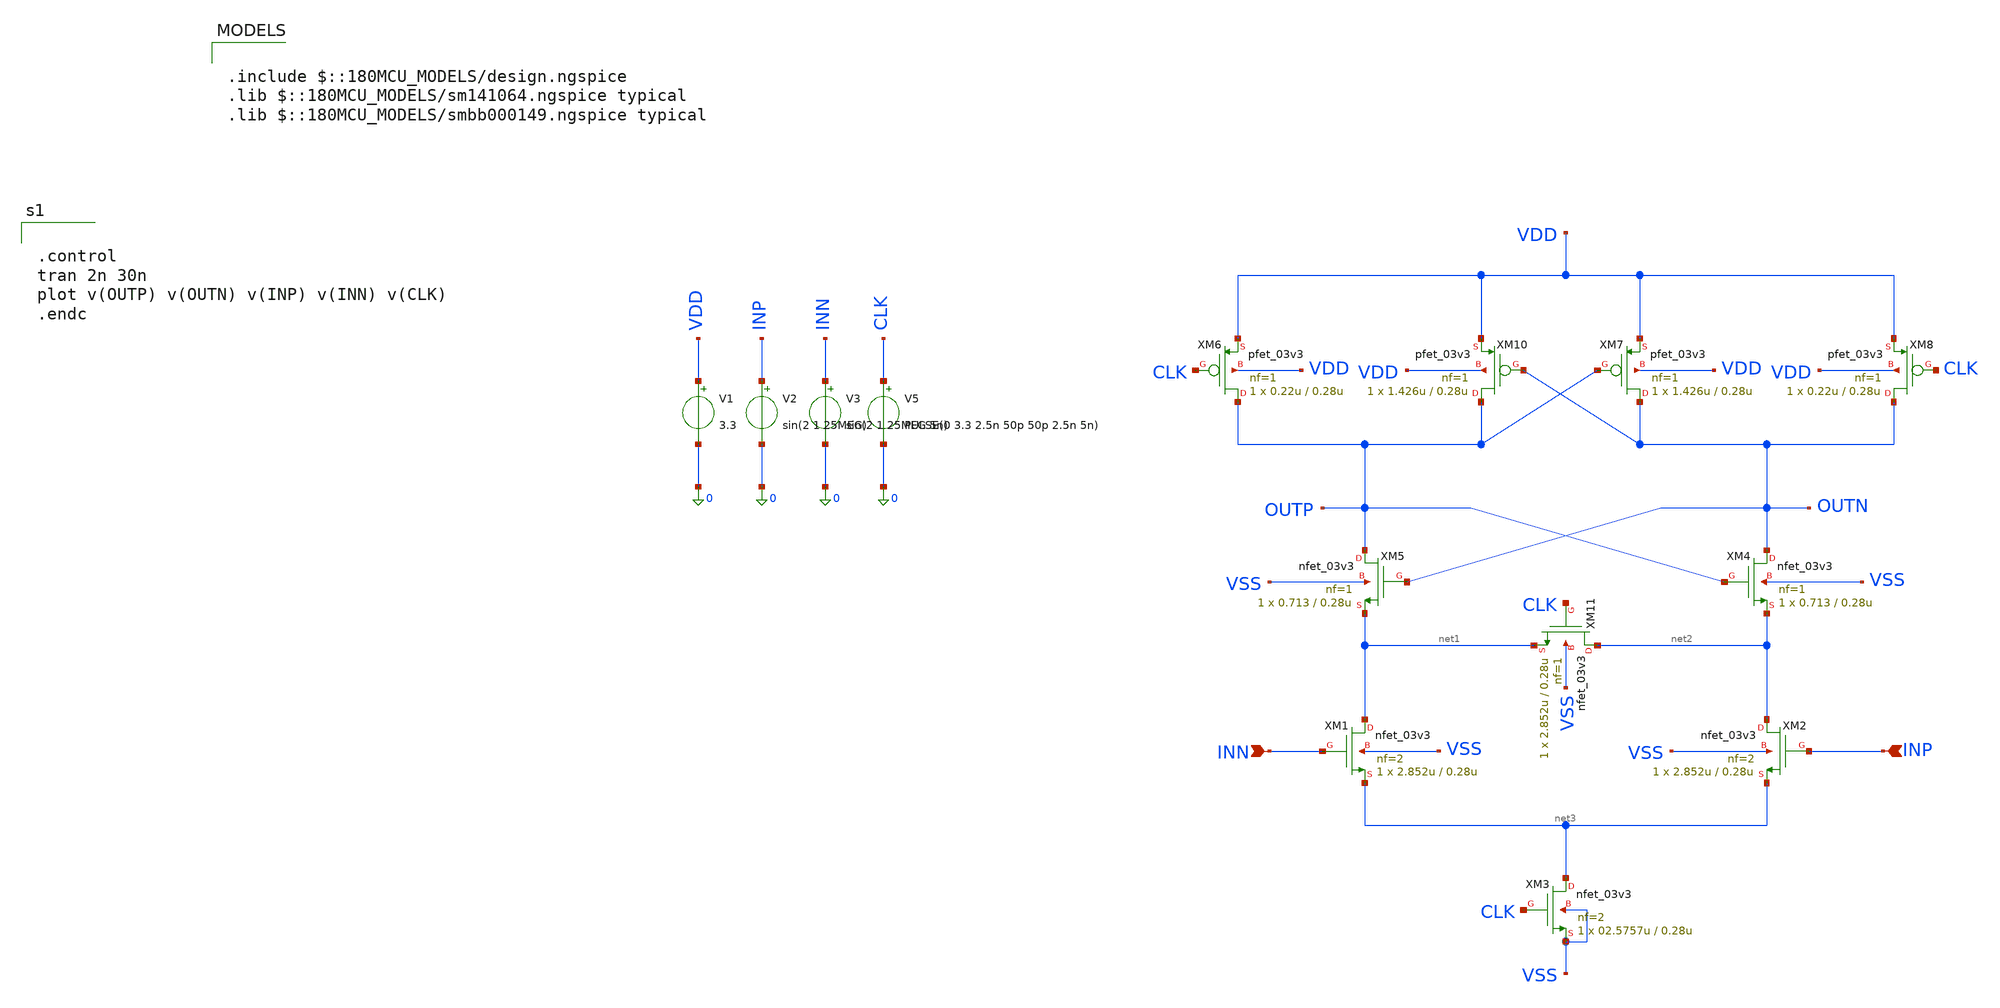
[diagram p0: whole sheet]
** sch_path: analog/blocks/Double_Tail_Comparator/size_sim.sch
**.subckt size_sim INN INP
*.ipin INN
*.ipin INP
XM1 net1 INN net3 VSS nfet_03v3 L=0.28u W=2.852u nf=2 ad='int((nf+1)/2) * W/nf * 0.18u' as='int((nf+2)/2) * W/nf * 0.18u'
+ pd='2*int((nf+1)/2) * (W/nf + 0.18u)' ps='2*int((nf+2)/2) * (W/nf + 0.18u)' nrd='0.18u / W' nrs='0.18u / W'
+ sa=0 sb=0 sd=0 m=1
XM2 net2 INP net3 VSS nfet_03v3 L=0.28u W=2.852u nf=2 ad='int((nf+1)/2) * W/nf * 0.18u' as='int((nf+2)/2) * W/nf * 0.18u'
+ pd='2*int((nf+1)/2) * (W/nf + 0.18u)' ps='2*int((nf+2)/2) * (W/nf + 0.18u)' nrd='0.18u / W' nrs='0.18u / W'
+ sa=0 sb=0 sd=0 m=1
XM3 net3 CLK VSS VSS nfet_03v3 L=0.28u W=02.5757u nf=2 ad='int((nf+1)/2) * W/nf * 0.18u' as='int((nf+2)/2) * W/nf * 0.18u'
+ pd='2*int((nf+1)/2) * (W/nf + 0.18u)' ps='2*int((nf+2)/2) * (W/nf + 0.18u)' nrd='0.18u / W' nrs='0.18u / W'
+ sa=0 sb=0 sd=0 m=1
XM4 OUTN OUTP net2 VSS nfet_03v3 L=0.28u W=0.713 nf=1 ad='int((nf+1)/2) * W/nf * 0.18u' as='int((nf+2)/2) * W/nf * 0.18u'
+ pd='2*int((nf+1)/2) * (W/nf + 0.18u)' ps='2*int((nf+2)/2) * (W/nf + 0.18u)' nrd='0.18u / W' nrs='0.18u / W'
+ sa=0 sb=0 sd=0 m=1
XM5 OUTP OUTN net1 VSS nfet_03v3 L=0.28u W=0.713 nf=1 ad='int((nf+1)/2) * W/nf * 0.18u' as='int((nf+2)/2) * W/nf * 0.18u'
+ pd='2*int((nf+1)/2) * (W/nf + 0.18u)' ps='2*int((nf+2)/2) * (W/nf + 0.18u)' nrd='0.18u / W' nrs='0.18u / W'
+ sa=0 sb=0 sd=0 m=1
XM6 OUTP CLK VDD VDD pfet_03v3 L=0.28u W=0.22u nf=1 ad='int((nf+1)/2) * W/nf * 0.18u' as='int((nf+2)/2) * W/nf * 0.18u'
+ pd='2*int((nf+1)/2) * (W/nf + 0.18u)' ps='2*int((nf+2)/2) * (W/nf + 0.18u)' nrd='0.18u / W' nrs='0.18u / W'
+ sa=0 sb=0 sd=0 m=1
XM7 OUTN OUTP VDD VDD pfet_03v3 L=0.28u W=1.426u nf=1 ad='int((nf+1)/2) * W/nf * 0.18u' as='int((nf+2)/2) * W/nf * 0.18u'
+ pd='2*int((nf+1)/2) * (W/nf + 0.18u)' ps='2*int((nf+2)/2) * (W/nf + 0.18u)' nrd='0.18u / W' nrs='0.18u / W'
+ sa=0 sb=0 sd=0 m=1
XM8 OUTN CLK VDD VDD pfet_03v3 L=0.28u W=0.22u nf=1 ad='int((nf+1)/2) * W/nf * 0.18u' as='int((nf+2)/2) * W/nf * 0.18u'
+ pd='2*int((nf+1)/2) * (W/nf + 0.18u)' ps='2*int((nf+2)/2) * (W/nf + 0.18u)' nrd='0.18u / W' nrs='0.18u / W'
+ sa=0 sb=0 sd=0 m=1
XM10 OUTP OUTN VDD VDD pfet_03v3 L=0.28u W=1.426u nf=1 ad='int((nf+1)/2) * W/nf * 0.18u' as='int((nf+2)/2) * W/nf * 0.18u'
+ pd='2*int((nf+1)/2) * (W/nf + 0.18u)' ps='2*int((nf+2)/2) * (W/nf + 0.18u)' nrd='0.18u / W' nrs='0.18u / W'
+ sa=0 sb=0 sd=0 m=1
XM11 net2 CLK net1 VSS nfet_03v3 L=0.28u W=2.852u nf=1 ad='int((nf+1)/2) * W/nf * 0.18u' as='int((nf+2)/2) * W/nf * 0.18u'
+ pd='2*int((nf+1)/2) * (W/nf + 0.18u)' ps='2*int((nf+2)/2) * (W/nf + 0.18u)' nrd='0.18u / W' nrs='0.18u / W'
+ sa=0 sb=0 sd=0 m=1
V1 VDD 0 3.3
V2 INP 0 sin(2 1 25MEG)
V3 INN 0 sin(2 1 25MEG 5n)
V5 CLK 0 PULSE(0 3.3 2.5n 50p 50p 2.5n 5n)
**** begin user architecture code

.include $::180MCU_MODELS/design.ngspice
.lib $::180MCU_MODELS/sm141064.ngspice typical
.lib $::180MCU_MODELS/smbb000149.ngspice typical



.control
tran 2n 30n
plot v(OUTP) v(OUTN) v(INP) v(INN) v(CLK)
.endc


**** end user architecture code
**.ends
.end
